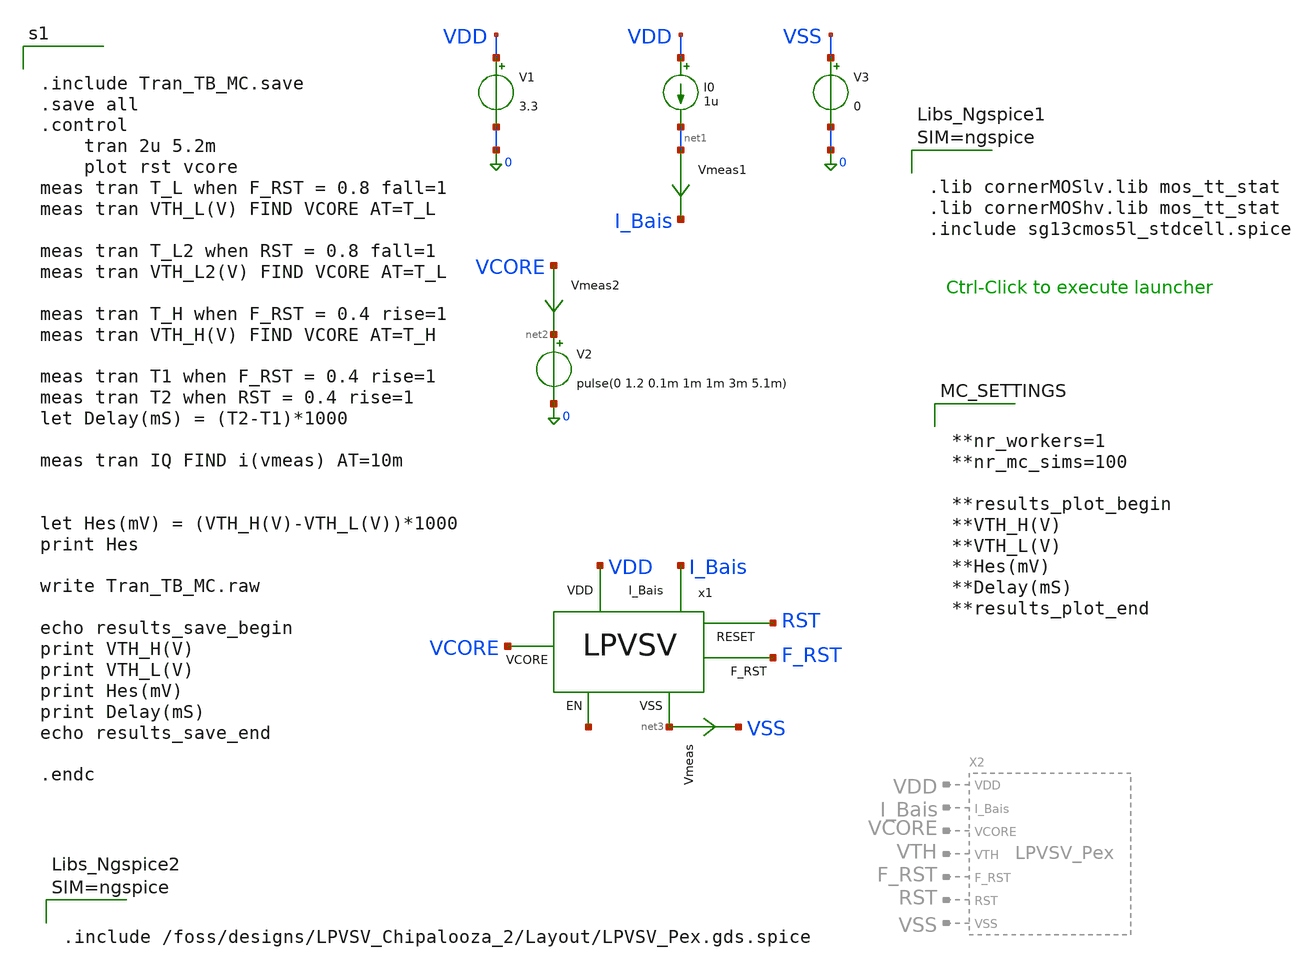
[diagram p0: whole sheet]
** sch_path: Simulation/Tran_TB_MC.sch
**.subckt Tran_TB_MC
V1 VDD 0 3.3
V2 net2 0 pulse(0 1.2 0.1m 1m 1m 3m 5.1m)
Vmeas net3 VSS 0
.save i(vmeas)
I0 VDD net1 1u
Vmeas1 net1 I_Bais 0
.save i(vmeas1)
Vmeas2 VCORE net2 0
.save i(vmeas2)
V3 VSS 0 0
x1 VDD VCORE I_Bais RST F_RST net3 net4 LPVSV
**** begin user architecture code



.lib cornerMOSlv.lib mos_tt_stat
.lib cornerMOShv.lib mos_tt_stat
.include sg13cmos5l_stdcell.spice





**nr_workers=1
**nr_mc_sims=100

**results_plot_begin
**VTH_H(V)
**VTH_L(V)
**Hes(mV)
**Delay(mS)
**results_plot_end




.include Tran_TB_MC.save
.save all
.control
	tran 2u 5.2m
	plot rst vcore
meas tran T_L when F_RST = 0.8 fall=1
meas tran VTH_L(V) FIND VCORE AT=T_L

meas tran T_L2 when RST = 0.8 fall=1
meas tran VTH_L2(V) FIND VCORE AT=T_L

meas tran T_H when F_RST = 0.4 rise=1
meas tran VTH_H(V) FIND VCORE AT=T_H

meas tran T1 when F_RST = 0.4 rise=1
meas tran T2 when RST = 0.4 rise=1
let Delay(mS) = (T2-T1)*1000

meas tran IQ FIND i(vmeas) AT=10m


let Hes(mV) = (VTH_H(V)-VTH_L(V))*1000
print Hes

write Tran_TB_MC.raw

echo results_save_begin
print VTH_H(V)
print VTH_L(V)
print Hes(mV)
print Delay(mS)
echo results_save_end

.endc





.include /foss/designs/LPVSV_Chipalooza_2/Layout/LPVSV_Pex.gds.spice



**** end user architecture code
**.ends
.end
